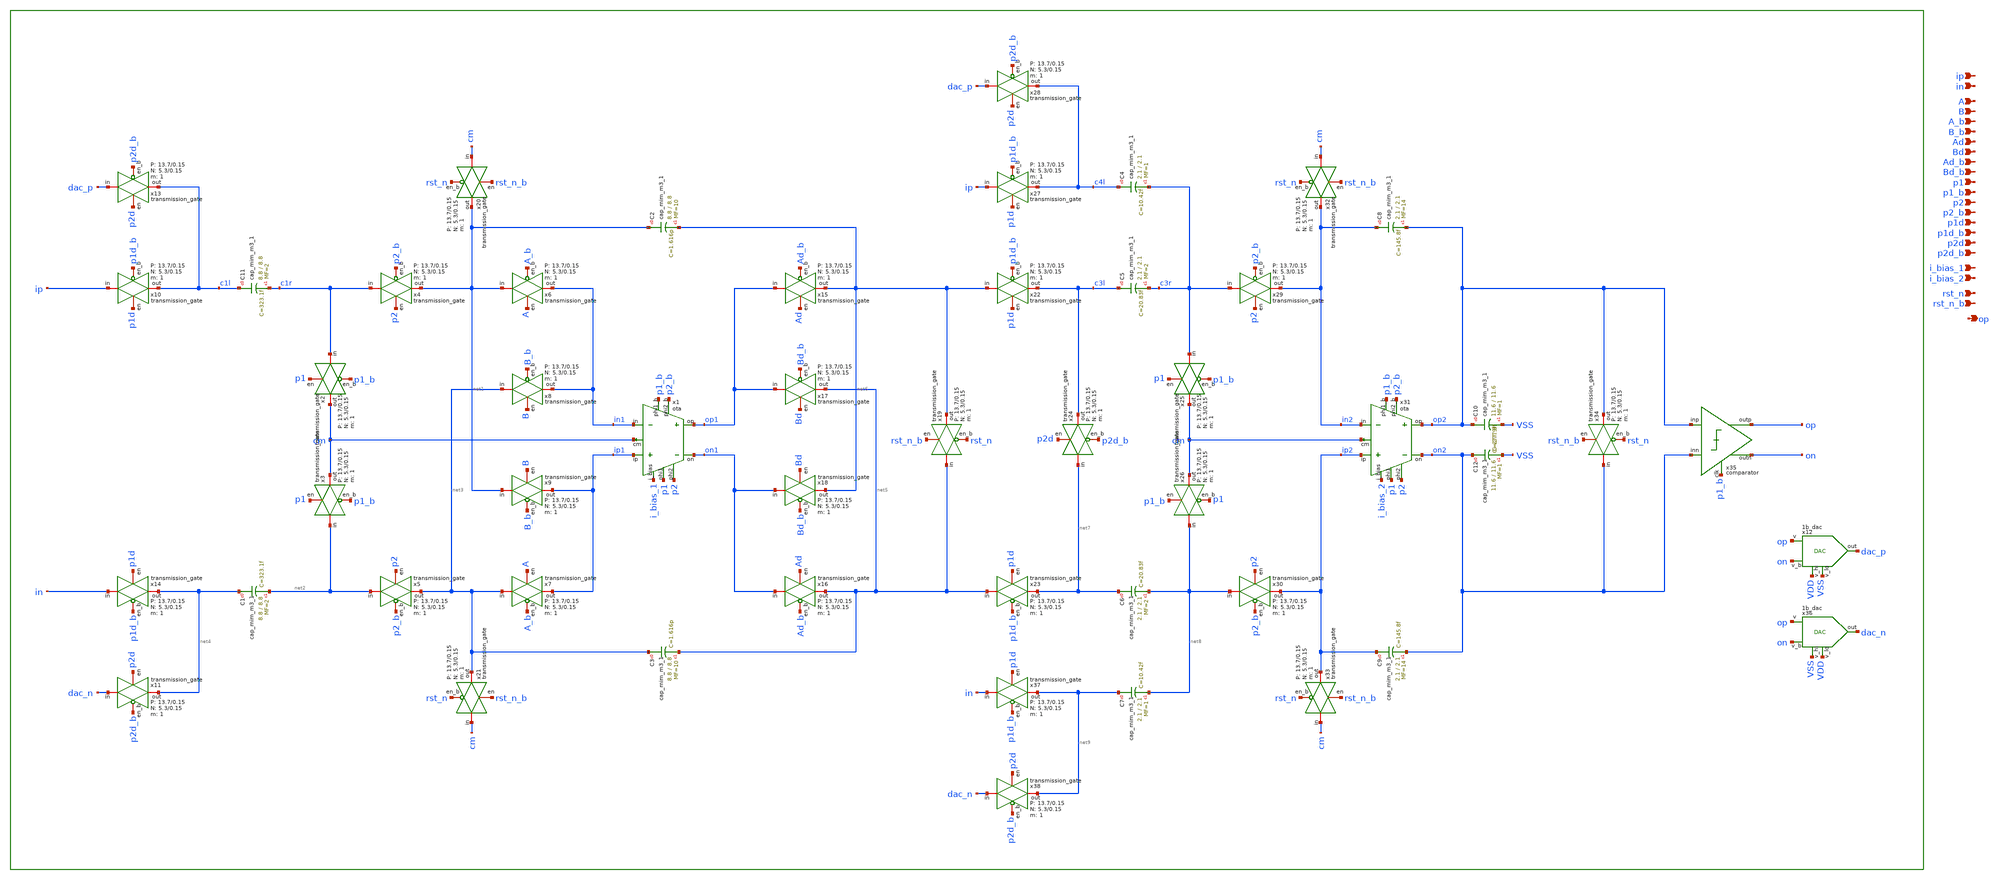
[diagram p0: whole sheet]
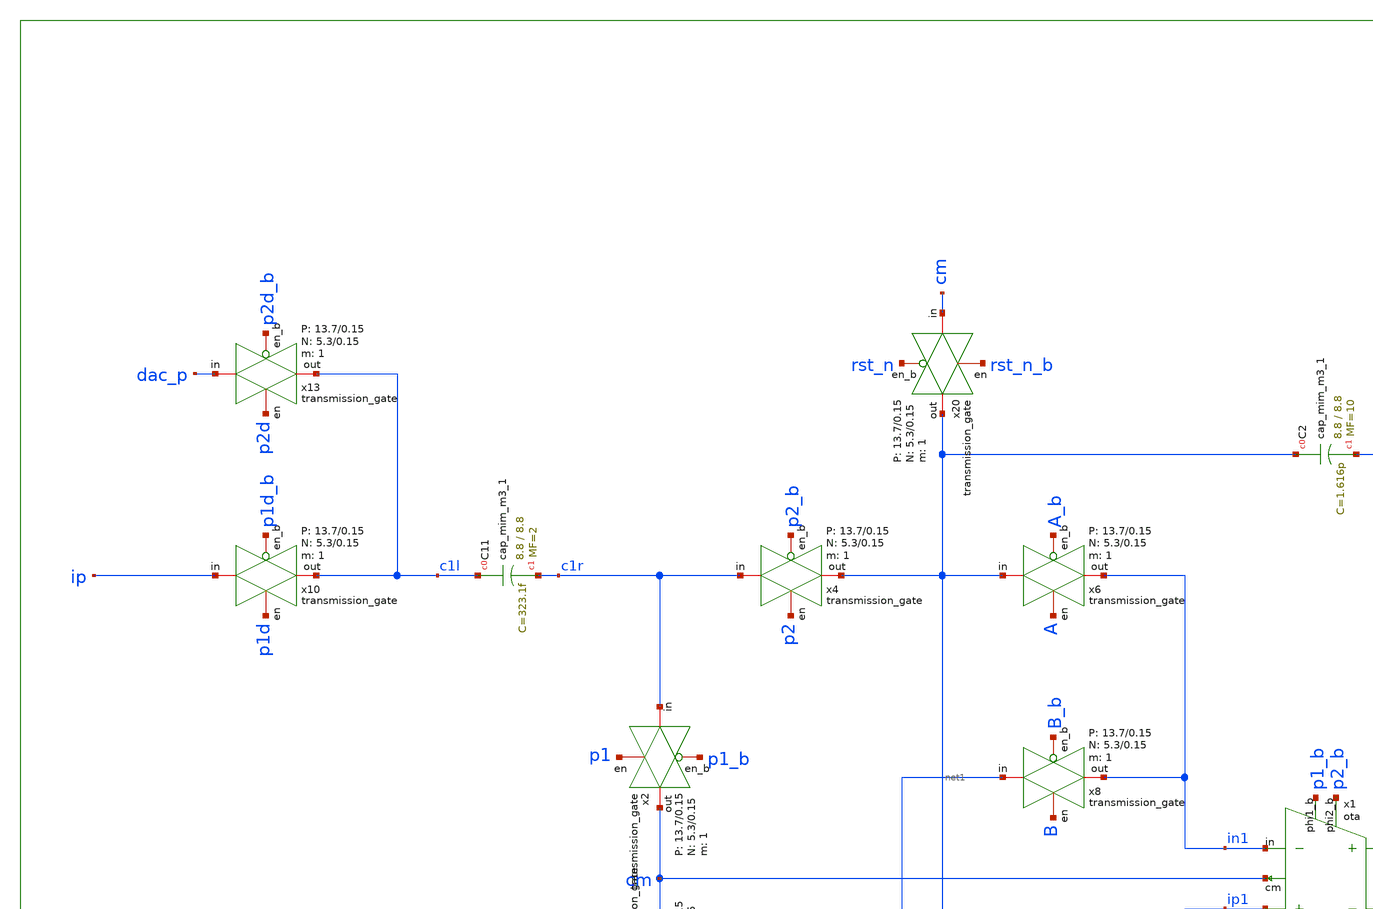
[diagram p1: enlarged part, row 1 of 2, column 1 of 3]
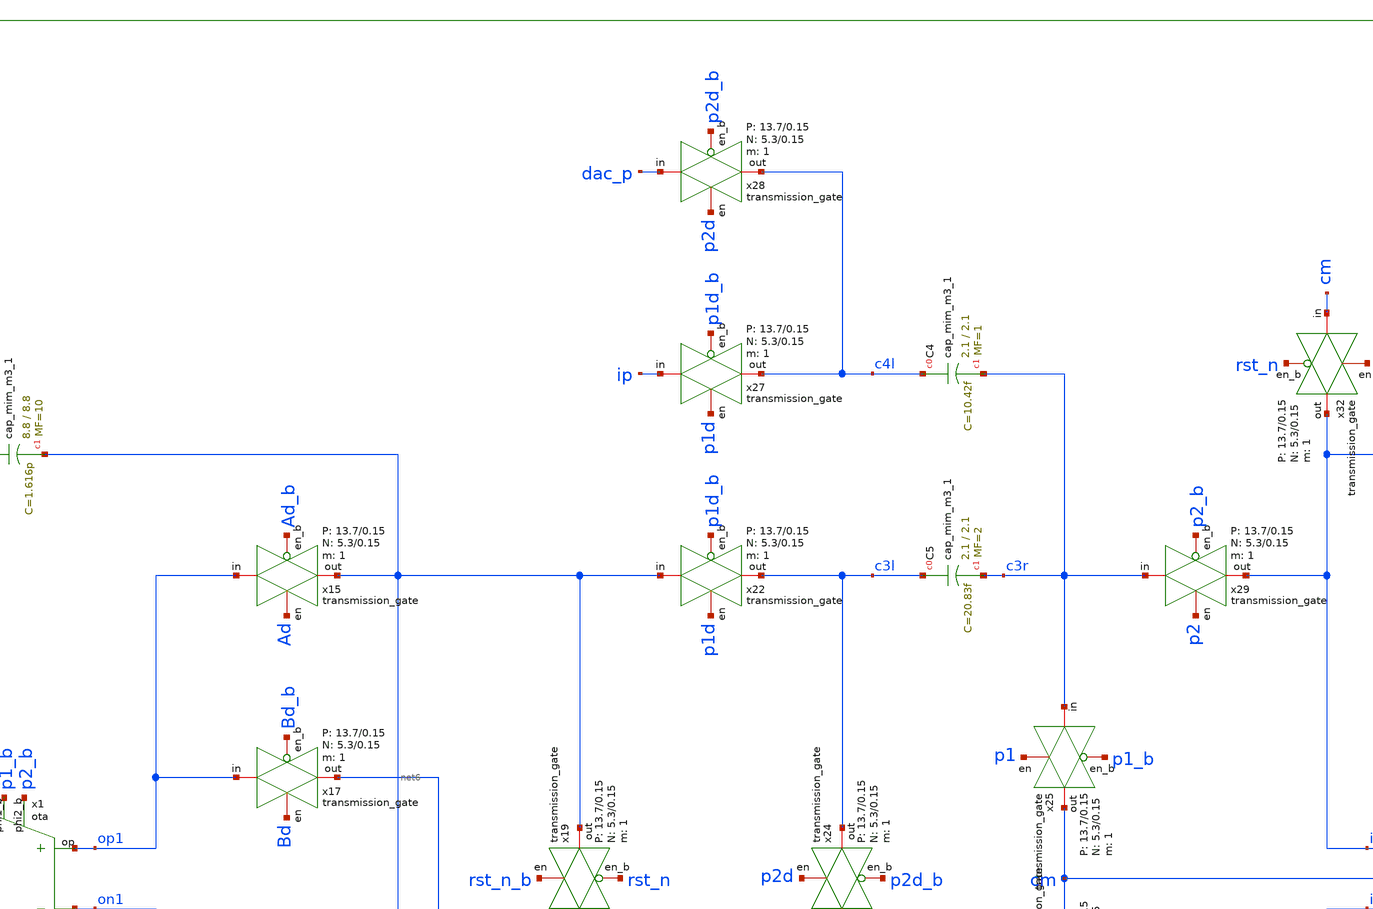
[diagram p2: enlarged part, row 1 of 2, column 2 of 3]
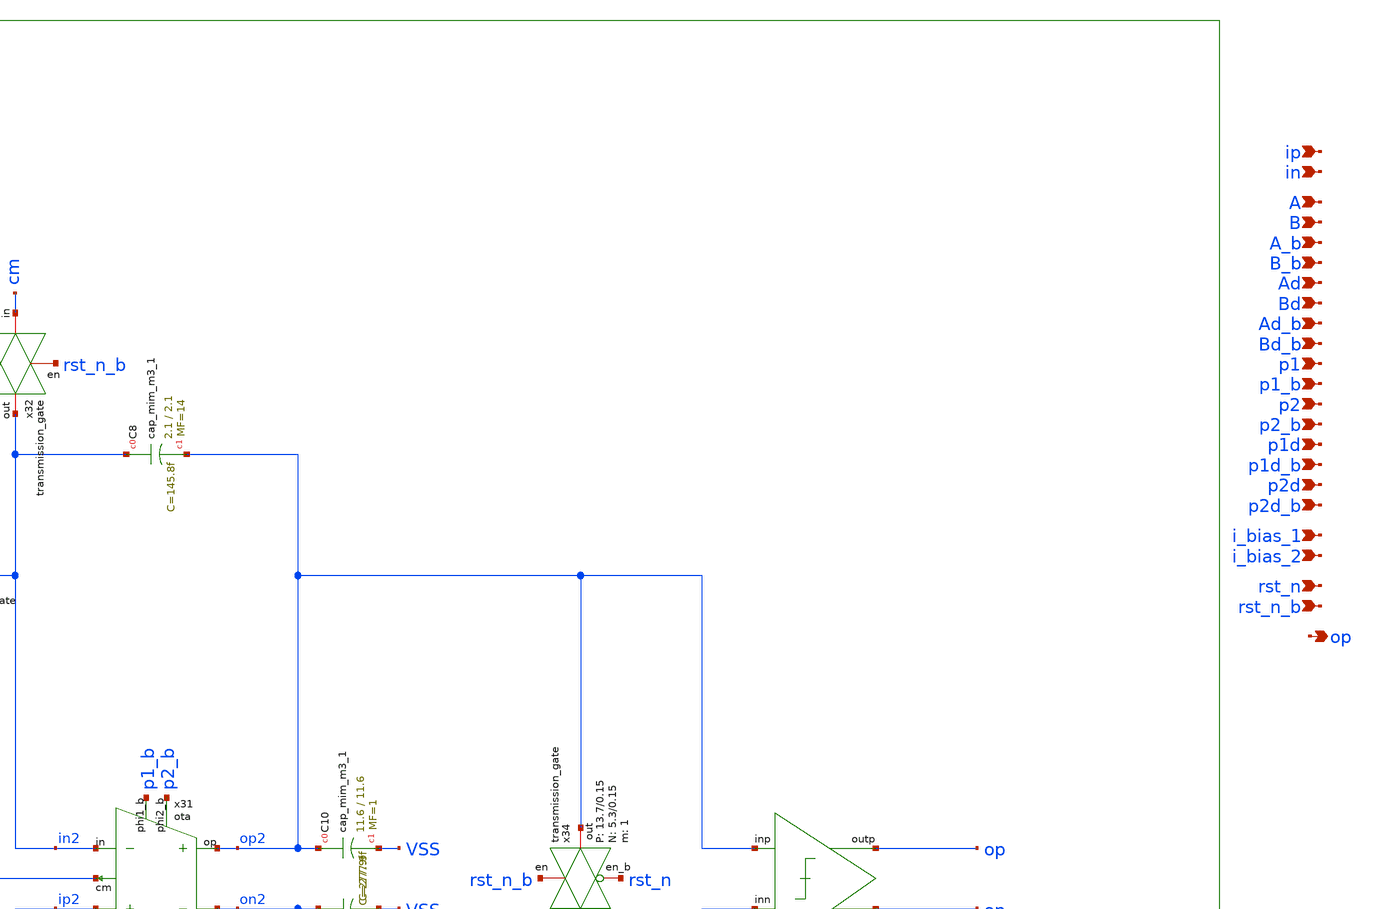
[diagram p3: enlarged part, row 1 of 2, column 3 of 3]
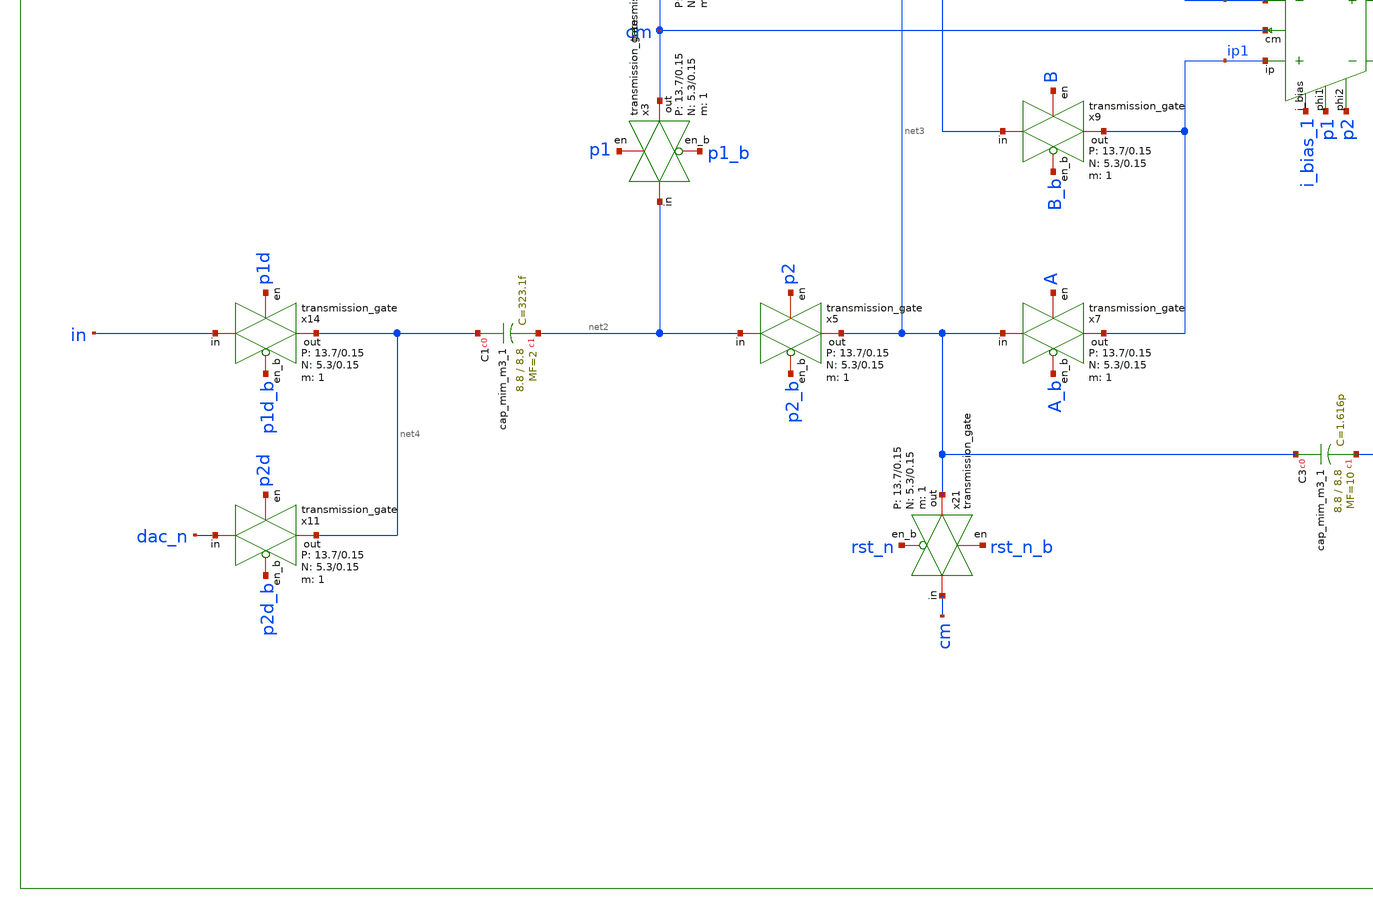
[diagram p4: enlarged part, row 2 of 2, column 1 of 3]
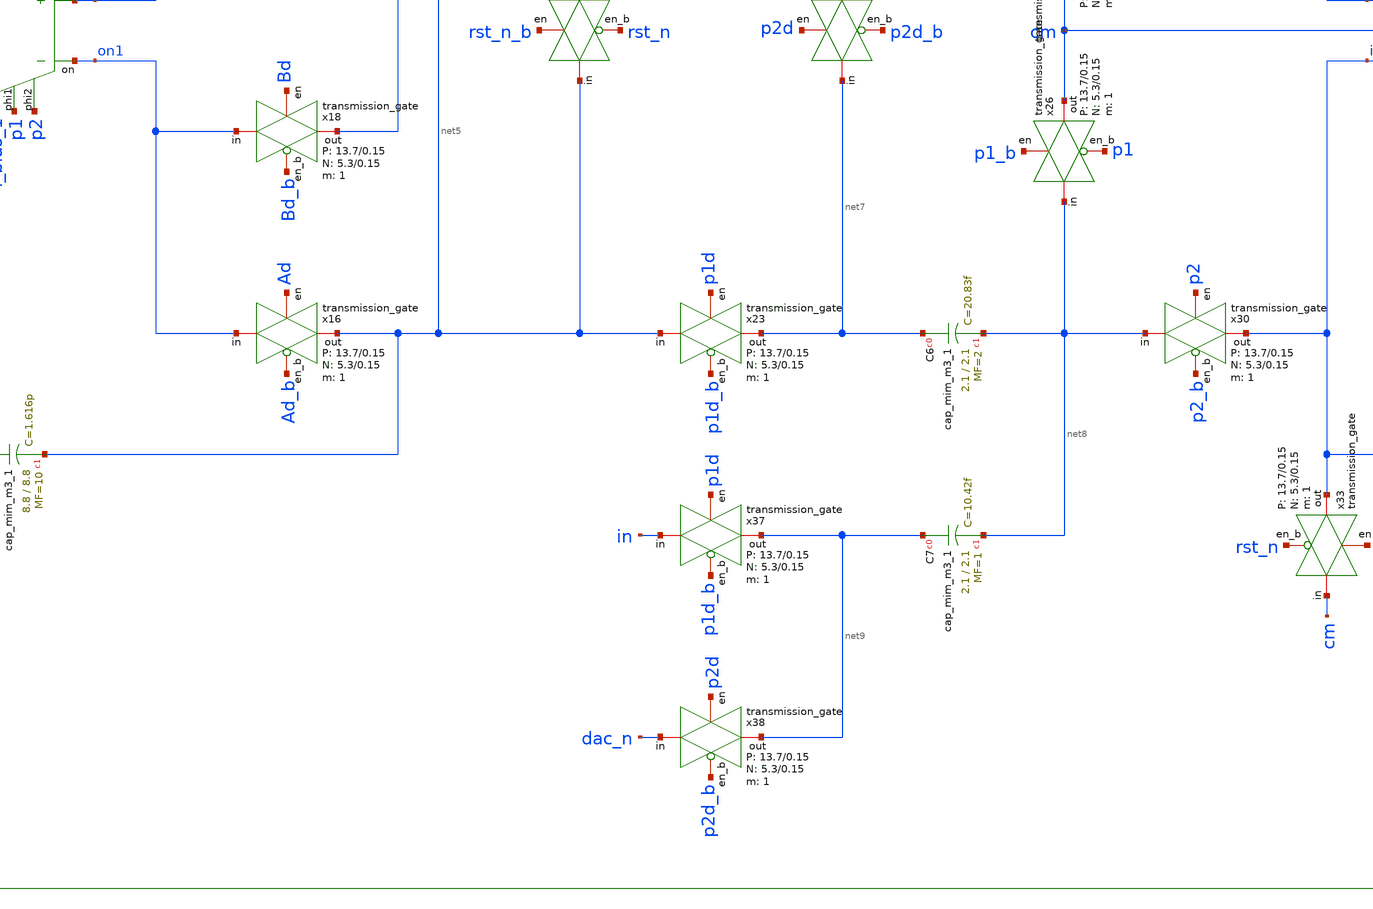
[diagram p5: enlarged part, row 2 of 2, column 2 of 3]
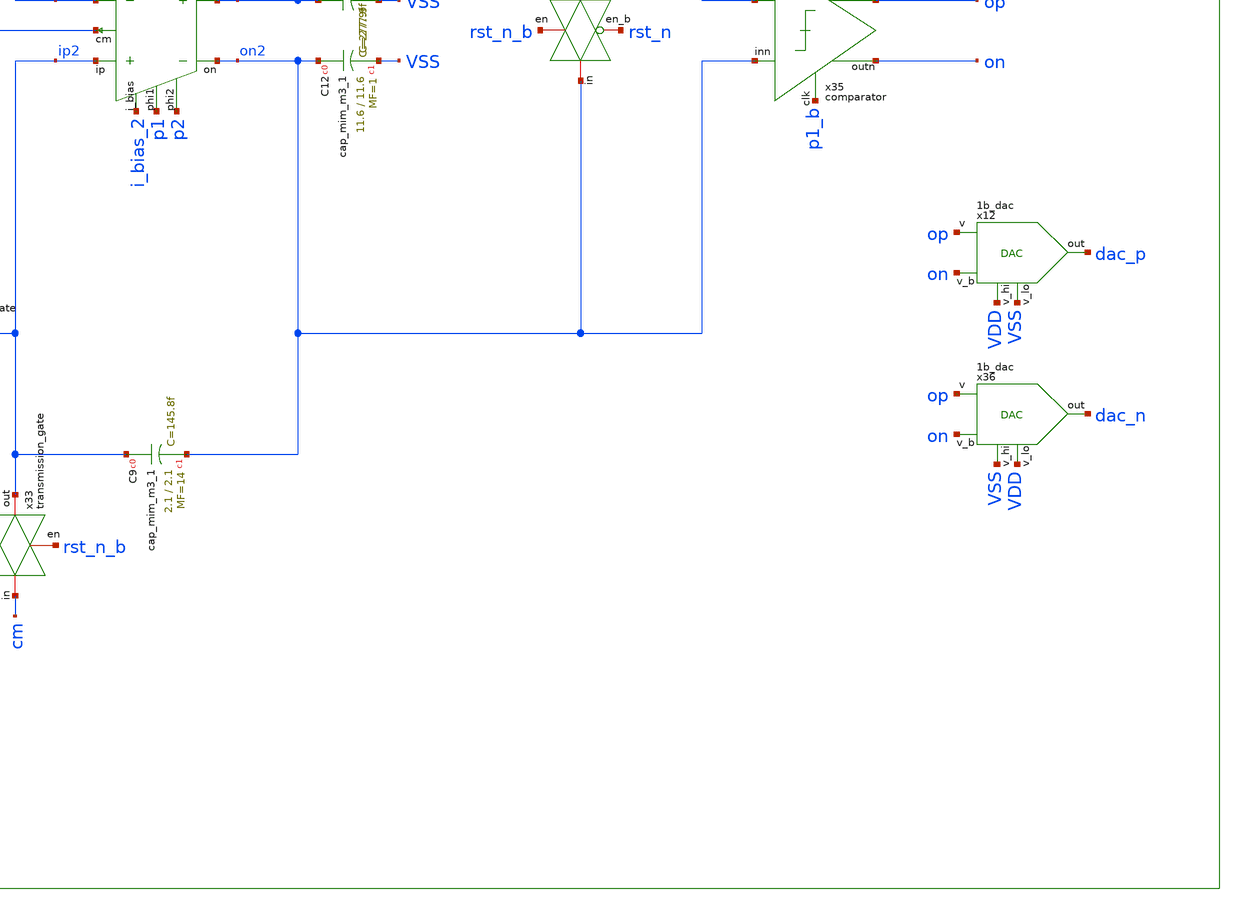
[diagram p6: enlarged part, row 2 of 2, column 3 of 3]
** sch_path: design/schematic/modulator.sch
**.subckt modulator ip in A B A_b B_b Ad Bd Ad_b Bd_b p1 p1_b p2 p2_b p1d p1d_b p2d p2d_b i_bias_1
*+ i_bias_2 rst_n rst_n_b op
*.ipin ip
*.ipin in
*.ipin A
*.ipin B
*.ipin A_b
*.ipin B_b
*.ipin Ad
*.ipin Bd
*.ipin Ad_b
*.ipin Bd_b
*.ipin p1
*.ipin p1_b
*.ipin p2
*.ipin p2_b
*.ipin p1d
*.ipin p1d_b
*.ipin p2d
*.ipin p2d_b
*.ipin i_bias_1
*.ipin i_bias_2
*.ipin rst_n
*.ipin rst_n_b
*.opin op
x1 i_bias_1 ip1 in1 p1 p1_b p2 p2_b op1 on1 cm 50 350 VDD VSS ota
x4 c1r net1 p2 p2_b VDD VSS 1 5.3 0.15 13.7 0.15 transmission_gate
x5 net2 net3 p2 p2_b VDD VSS 1 5.3 0.15 13.7 0.15 transmission_gate
x2 c1r cm p1 p1_b VDD VSS 1 5.3 0.15 13.7 0.15 transmission_gate
x3 net2 cm p1 p1_b VDD VSS 1 5.3 0.15 13.7 0.15 transmission_gate
x10 ip c1l p1d p1d_b VDD VSS 1 5.3 0.15 13.7 0.15 transmission_gate
x11 dac_n net4 p2d p2d_b VDD VSS 1 5.3 0.15 13.7 0.15 transmission_gate
x12 VDD VSS op dac_p on VDD VSS 1b_dac
x13 dac_p c1l p2d p2d_b VDD VSS 1 5.3 0.15 13.7 0.15 transmission_gate
x14 in net4 p1d p1d_b VDD VSS 1 5.3 0.15 13.7 0.15 transmission_gate
x19 net5 net6 rst_n_b rst_n VDD VSS 1 5.3 0.15 13.7 0.15 transmission_gate
x20 cm net1 rst_n_b rst_n VDD VSS 1 5.3 0.15 13.7 0.15 transmission_gate
x21 cm net3 rst_n_b rst_n VDD VSS 1 5.3 0.15 13.7 0.15 transmission_gate
x22 net6 c3l p1d p1d_b VDD VSS 1 5.3 0.15 13.7 0.15 transmission_gate
x23 net5 net7 p1d p1d_b VDD VSS 1 5.3 0.15 13.7 0.15 transmission_gate
x24 net7 c3l p2d p2d_b VDD VSS 1 5.3 0.15 13.7 0.15 transmission_gate
x25 c3r cm p1 p1_b VDD VSS 1 5.3 0.15 13.7 0.15 transmission_gate
x26 net8 cm p1_b p1 VDD VSS 1 5.3 0.15 13.7 0.15 transmission_gate
x27 ip c4l p1d p1d_b VDD VSS 1 5.3 0.15 13.7 0.15 transmission_gate
x28 dac_p c4l p2d p2d_b VDD VSS 1 5.3 0.15 13.7 0.15 transmission_gate
x29 c3r in2 p2 p2_b VDD VSS 1 5.3 0.15 13.7 0.15 transmission_gate
x30 net8 ip2 p2 p2_b VDD VSS 1 5.3 0.15 13.7 0.15 transmission_gate
x31 i_bias_2 ip2 in2 p1 p1_b p2 p2_b op2 on2 cm 50 350 VDD VSS ota
x32 cm in2 rst_n_b rst_n VDD VSS 1 5.3 0.15 13.7 0.15 transmission_gate
x33 cm ip2 rst_n_b rst_n VDD VSS 1 5.3 0.15 13.7 0.15 transmission_gate
x34 on2 op2 rst_n_b rst_n VDD VSS 1 5.3 0.15 13.7 0.15 transmission_gate
x35 op2 on2 op p1_b on VDD VSS comparator
x36 VSS VDD op dac_n on VDD VSS 1b_dac
x37 in net9 p1d p1d_b VDD VSS 1 5.3 0.15 13.7 0.15 transmission_gate
x38 dac_n net9 p2d p2d_b VDD VSS 1 5.3 0.15 13.7 0.15 transmission_gate
XC11 c1l c1r sky130_fd_pr__cap_mim_m3_1 W=8.8 L=8.8 MF=2 m=2
XC1 net4 net2 sky130_fd_pr__cap_mim_m3_1 W=8.8 L=8.8 MF=2 m=2
XC2 net1 net6 sky130_fd_pr__cap_mim_m3_1 W=8.8 L=8.8 MF=10 m=10
XC3 net3 net5 sky130_fd_pr__cap_mim_m3_1 W=8.8 L=8.8 MF=10 m=10
XC4 c4l c3r sky130_fd_pr__cap_mim_m3_1 W=2.1 L=2.1 MF=1 m=1
XC5 c3l c3r sky130_fd_pr__cap_mim_m3_1 W=2.1 L=2.1 MF=2 m=2
XC6 net7 net8 sky130_fd_pr__cap_mim_m3_1 W=2.1 L=2.1 MF=2 m=2
XC7 net9 net8 sky130_fd_pr__cap_mim_m3_1 W=2.1 L=2.1 MF=1 m=1
XC8 in2 op2 sky130_fd_pr__cap_mim_m3_1 W=2.1 L=2.1 MF=14 m=14
XC9 ip2 on2 sky130_fd_pr__cap_mim_m3_1 W=2.1 L=2.1 MF=14 m=14
XC10 op2 VSS sky130_fd_pr__cap_mim_m3_1 W=11.6 L=11.6 MF=1 m=1
XC12 on2 VSS sky130_fd_pr__cap_mim_m3_1 W=11.6 L=11.6 MF=1 m=1
x6 net1 in1 A A_b VDD VSS 1 5.3 0.15 13.7 0.15 transmission_gate
x7 net3 ip1 A A_b VDD VSS 1 5.3 0.15 13.7 0.15 transmission_gate
x8 net3 in1 B B_b VDD VSS 1 5.3 0.15 13.7 0.15 transmission_gate
x9 net1 ip1 B B_b VDD VSS 1 5.3 0.15 13.7 0.15 transmission_gate
x15 op1 net6 Ad Ad_b VDD VSS 1 5.3 0.15 13.7 0.15 transmission_gate
x16 on1 net5 Ad Ad_b VDD VSS 1 5.3 0.15 13.7 0.15 transmission_gate
x17 op1 net5 Bd Bd_b VDD VSS 1 5.3 0.15 13.7 0.15 transmission_gate
x18 on1 net6 Bd Bd_b VDD VSS 1 5.3 0.15 13.7 0.15 transmission_gate
**.ends
.end
